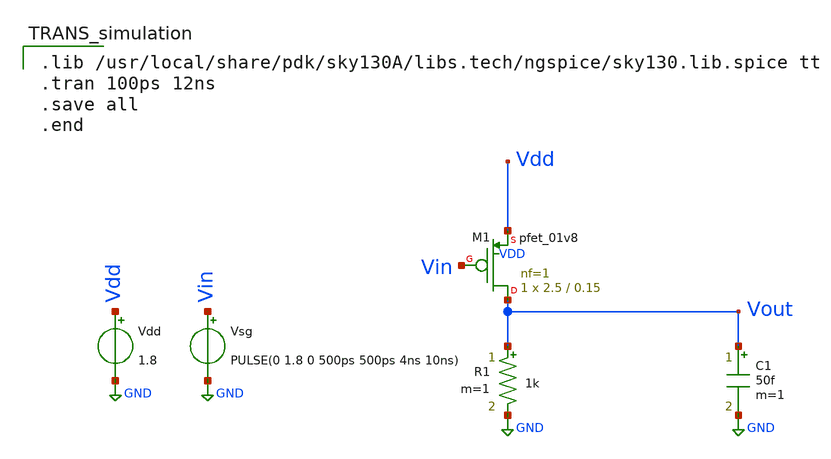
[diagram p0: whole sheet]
** sch_path: Design-and-analysis-of-CMOS-ineverter/XSCHEM FILES/PMOSs1w0.sch
**.subckt PMOSs1w0
XM1 Vout Vin Vdd VDD sky130_fd_pr__pfet_01v8 L=0.15 W=2.5 nf=1 ad='int((nf+1)/2) * W/nf * 0.29' as='int((nf+2)/2) * W/nf * 0.29'
+ pd='2*int((nf+1)/2) * (W/nf + 0.29)' ps='2*int((nf+2)/2) * (W/nf + 0.29)' nrd='0.29 / W' nrs='0.29 / W'
+ sa=0 sb=0 sd=0 mult=1 m=1
Vdd Vdd GND 1.8
Vsg Vin GND PULSE(0 1.8 0 500ps 500ps 4ns 10ns)
C1 Vout GND 50f m=1
R1 Vout GND 1k m=1
**** begin user architecture code

.lib /usr/local/share/pdk/sky130A/libs.tech/ngspice/sky130.lib.spice tt
.tran 100ps 12ns
.save all
.end

**** end user architecture code
**.ends
.GLOBAL GND
.end
